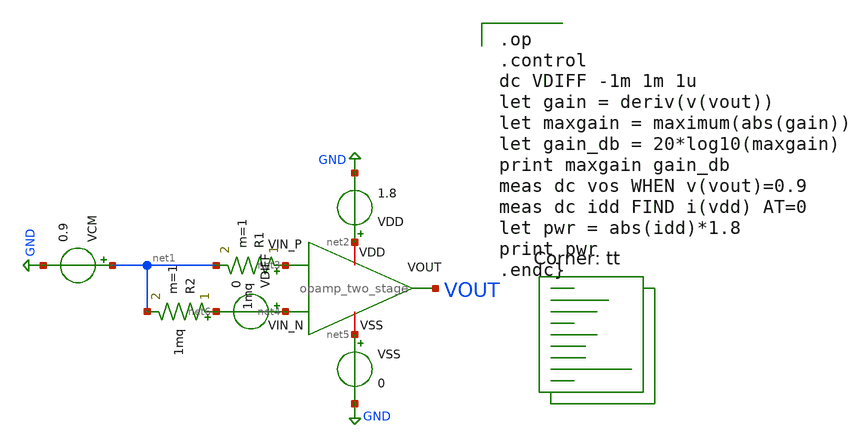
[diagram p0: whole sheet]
** sch_path: analog/bootcamp_opamp/schematics/tb_dc_analysis.sch
**.subckt tb_dc_analysis
x1 net2 VOUT net3 net4 net5 opamp_two_stage
VSS net5 GND 0
VDD net2 GND 1.8
VCM net1 GND 0.9
VDIFF net4 net6 0
R1 net3 net1 1mq m=1
R2 net6 net1 1mq m=1
**** begin user architecture code

.op
.control
dc VDIFF -1m 1m 1u
let gain = deriv(v(vout))
let maxgain = maximum(abs(gain))
let gain_db = 20*log10(maxgain)
print maxgain gain_db
meas dc vos WHEN v(vout)=0.9
meas dc idd FIND i(vdd) AT=0
let pwr = abs(idd)*1.8
print pwr
.endc}

.lib $::SKYWATER_MODELS/sky130.lib.spice tt
**** end user architecture code
**.ends
.GLOBAL GND
.end
